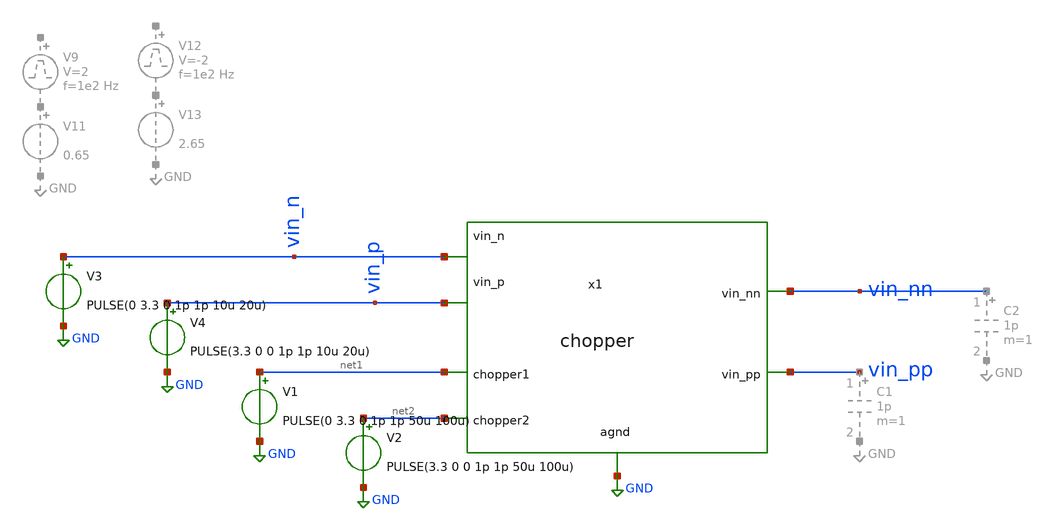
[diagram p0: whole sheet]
** sch_path: ABC123_SDC/design_data/xschem/CHOPPER/chopper_tb.sch
**.subckt chopper_tb
x1 vin_n vin_p GND net1 net2 vin_nn vin_pp chopper
V3 vin_n GND PULSE(0 3.3 0 1p 1p 10u 20u)
V4 vin_p GND PULSE(3.3 0 0 1p 1p 10u 20u)
V1 net1 GND PULSE(0 3.3 0 1p 1p 50u 100u)
V2 net2 GND PULSE(3.3 0 0 1p 1p 50u 100u)
**** begin user architecture code

.include $::180MCU_MODELS/design.ngspice
.lib $::180MCU_MODELS/sm141064.ngspice typical
.lib $::180MCU_MODELS/sm141064.ngspice cap_mim
.lib $::180MCU_MODELS/sm141064.ngspice res_typical
.lib $::180MCU_MODELS/sm141064.ngspice moscap_typical
.lib $::180MCU_MODELS/sm141064.ngspice mimcap_typical
* .lib $::180MCU_MODELS/sm141064.ngspice res_statistical



.save v(DOUT_CLOAD)
*.OPTION CSHUNT=0.01e-12
.OPTION ABSTOL=1e-15.
.OPTION GMIN=1.0e-12.
.OPTION ITL1=1e5
.OPTION RSHUNT=1e12
.OPTION RELTOL=1e-5

.option TEMP=27
.control
  save all
  tran 1n 2m

  plot vin_n vin_p vin_nn vin_pp
.endc


**** end user architecture code
**.ends

* expanding   symbol:  SDC_techmigration_May2026/SDC_GF/SDC_pts/chopper.sym # of pins=7
** sym_path: ABC123_SDC/design_data/xschem/CHOPPER/chopper.sym
** sch_path: ABC123_SDC/design_data/xschem/CHOPPER/chopper.sch
.subckt chopper vin_n vin_p agnd chopper1 chopper2 vin_nn vin_pp
*.ipin vin_n
*.ipin vin_p
*.ipin agnd
*.ipin chopper1
*.ipin chopper2
*.opin vin_nn
*.opin vin_pp
XM2 vin_n chopper1 vin_nn agnd nfet_03v3 L=0.28u W=6u nf=1 ad='int((nf+1)/2) * W/nf * 0.18u' as='int((nf+2)/2) * W/nf * 0.18u'
+ pd='2*int((nf+1)/2) * (W/nf + 0.18u)' ps='2*int((nf+2)/2) * (W/nf + 0.18u)' nrd='0.18u / W' nrs='0.18u / W'
+ sa=0 sb=0 sd=0 m=10
XM1 vin_n chopper2 vin_pp agnd nfet_03v3 L=0.28u W=6u nf=1 ad='int((nf+1)/2) * W/nf * 0.18u' as='int((nf+2)/2) * W/nf * 0.18u'
+ pd='2*int((nf+1)/2) * (W/nf + 0.18u)' ps='2*int((nf+2)/2) * (W/nf + 0.18u)' nrd='0.18u / W' nrs='0.18u / W'
+ sa=0 sb=0 sd=0 m=10
XM3 vin_p chopper2 vin_nn agnd nfet_03v3 L=0.28u W=6u nf=1 ad='int((nf+1)/2) * W/nf * 0.18u' as='int((nf+2)/2) * W/nf * 0.18u'
+ pd='2*int((nf+1)/2) * (W/nf + 0.18u)' ps='2*int((nf+2)/2) * (W/nf + 0.18u)' nrd='0.18u / W' nrs='0.18u / W'
+ sa=0 sb=0 sd=0 m=10
XM4 vin_p chopper1 vin_pp agnd nfet_03v3 L=0.28u W=6u nf=1 ad='int((nf+1)/2) * W/nf * 0.18u' as='int((nf+2)/2) * W/nf * 0.18u'
+ pd='2*int((nf+1)/2) * (W/nf + 0.18u)' ps='2*int((nf+2)/2) * (W/nf + 0.18u)' nrd='0.18u / W' nrs='0.18u / W'
+ sa=0 sb=0 sd=0 m=10
.ends

.GLOBAL GND
.end
